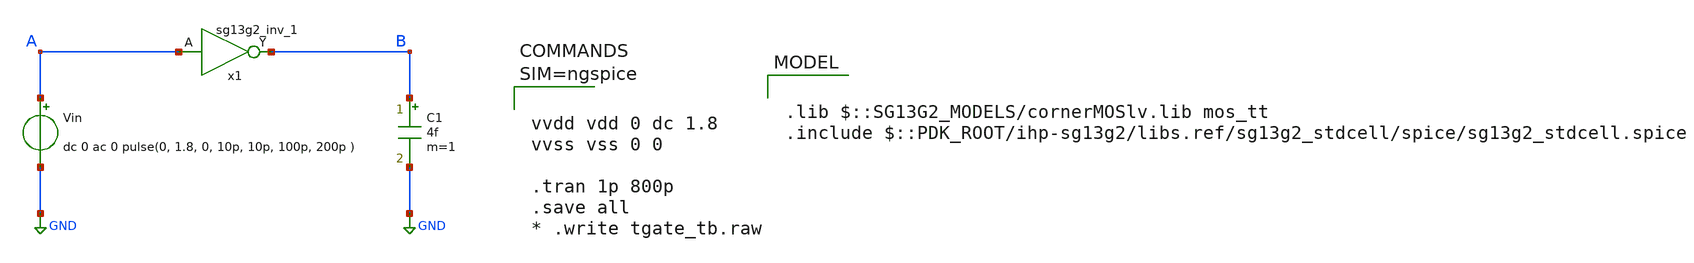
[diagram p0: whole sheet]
** sch_path: ngspice_cosim_tgate/tgate_tb.sch
**.subckt tgate_tb
Vin A GND dc 0 ac 0 pulse(0, 1.8, 0, 10p, 10p, 100p, 200p )
x1 B A VDD VSS sg13g2_inv_1
C1 B GND 4f m=1
**** begin user architecture code



vvdd vdd 0 dc 1.8
vvss vss 0 0

.tran 1p 800p
.save all
* .write tgate_tb.raw




.lib $::SG13G2_MODELS/cornerMOSlv.lib mos_tt
.include $::PDK_ROOT/ihp-sg13g2/libs.ref/sg13g2_stdcell/spice/sg13g2_stdcell.spice

**** end user architecture code
**.ends

* expanding   symbol:  sg13g2_stdcells/sg13g2_inv_1.sym # of pins=2
** sym_path: sg13g2_stdcells/sg13g2_inv_1.sym
** sch_path: sg13g2_stdcells/sg13g2_inv_1.sch
.subckt sg13g2_inv_1 Y A VDD VSS
*.opin Y
*.ipin A
*.iopin VDD
*.iopin VSS
XM1 Y A VSS VSS sg13_lv_nmos w=740.00n l=130.00n ng=1 m=1 mm_ok=1
XM2 Y A VDD VDD sg13_lv_pmos w=1.12u l=130.00n ng=1 m=1 mm_ok=1
.ends

.GLOBAL GND
.end
